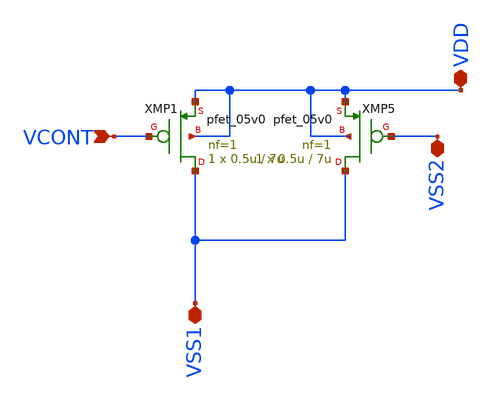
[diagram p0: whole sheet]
** sch_path: xschem/vco/vco_vcont_forlvs.sch
**.subckt vco_vcont_forlvs VDD VCONT VSS1 VSS2
*.iopin VDD
*.ipin VCONT
*.iopin VSS1
*.iopin VSS2
XMP1 VSS1 VCONT VDD VDD pfet_05v0 L=7u W=0.5u nf=1 ad='int((nf+1)/2) * W/nf * 0.18u' as='int((nf+2)/2) * W/nf * 0.18u'
+ pd='2*int((nf+1)/2) * (W/nf + 0.18u)' ps='2*int((nf+2)/2) * (W/nf + 0.18u)' nrd='0.18u / W' nrs='0.18u / W'
+ sa=0 sb=0 sd=0 m=1
XMP5 VSS1 VSS2 VDD VDD pfet_05v0 L=7u W=0.5u nf=1 ad='int((nf+1)/2) * W/nf * 0.18u' as='int((nf+2)/2) * W/nf * 0.18u'
+ pd='2*int((nf+1)/2) * (W/nf + 0.18u)' ps='2*int((nf+2)/2) * (W/nf + 0.18u)' nrd='0.18u / W' nrs='0.18u / W'
+ sa=0 sb=0 sd=0 m=1
**.ends
.end
